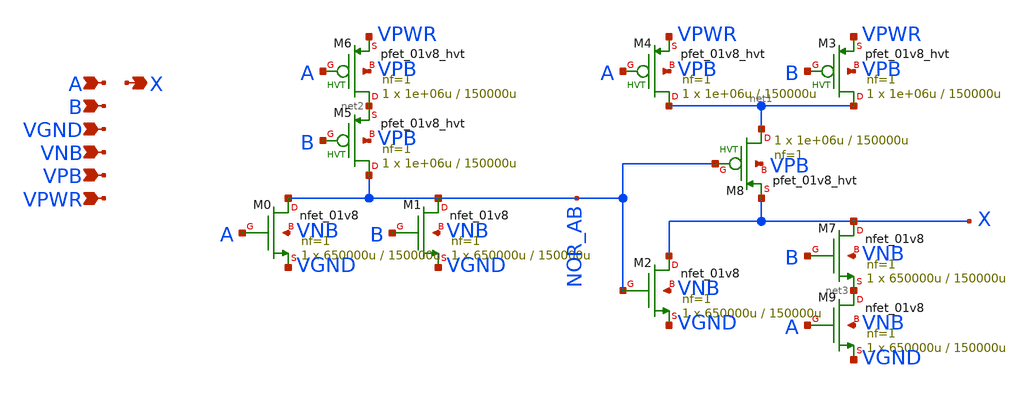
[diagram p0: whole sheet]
** sch_path: schematics/xor2/sky130_fd_sc_hd__xor2_1.sch
**.subckt sky130_fd_sc_hd__xor2_1 A B VGND VNB VPB VPWR X
*.ipin A
*.ipin B
*.ipin VGND
*.ipin VNB
*.ipin VPB
*.ipin VPWR
*.opin X
XM4 net1 A VPWR VPB sky130_fd_pr__pfet_01v8_hvt L=150000u W=1e+06u nf=1 ad='int((1 + 1)/2) * 1e+06u / 1 * 0.29'
+ as='int((1 + 2)/2) * 1e+06u / 1 * 0.29' pd='2*int((1 + 1)/2) * (1e+06u / 1 + 0.29)' ps='2*int((1 + 2)/2) * (1e+06u / 1 + 0.29)'
+ nrd='0.29 / 1e+06u ' nrs='0.29 / 1e+06u ' sa=0 sb=0 sd=0 mult=1 m=1
XM6 net2 A VPWR VPB sky130_fd_pr__pfet_01v8_hvt L=150000u W=1e+06u nf=1 ad='int((1 + 1)/2) * 1e+06u / 1 * 0.29'
+ as='int((1 + 2)/2) * 1e+06u / 1 * 0.29' pd='2*int((1 + 1)/2) * (1e+06u / 1 + 0.29)' ps='2*int((1 + 2)/2) * (1e+06u / 1 + 0.29)'
+ nrd='0.29 / 1e+06u ' nrs='0.29 / 1e+06u ' sa=0 sb=0 sd=0 mult=1 m=1
XM8 net1 NOR_AB X VPB sky130_fd_pr__pfet_01v8_hvt L=150000u W=1e+06u nf=1 ad='int((1 + 1)/2) * 1e+06u / 1 * 0.29'
+ as='int((1 + 2)/2) * 1e+06u / 1 * 0.29' pd='2*int((1 + 1)/2) * (1e+06u / 1 + 0.29)' ps='2*int((1 + 2)/2) * (1e+06u / 1 + 0.29)'
+ nrd='0.29 / 1e+06u ' nrs='0.29 / 1e+06u ' sa=0 sb=0 sd=0 mult=1 m=1
XM3 net1 B VPWR VPB sky130_fd_pr__pfet_01v8_hvt L=150000u W=1e+06u nf=1 ad='int((1 + 1)/2) * 1e+06u / 1 * 0.29'
+ as='int((1 + 2)/2) * 1e+06u / 1 * 0.29' pd='2*int((1 + 1)/2) * (1e+06u / 1 + 0.29)' ps='2*int((1 + 2)/2) * (1e+06u / 1 + 0.29)'
+ nrd='0.29 / 1e+06u ' nrs='0.29 / 1e+06u ' sa=0 sb=0 sd=0 mult=1 m=1
XM5 NOR_AB B net2 VPB sky130_fd_pr__pfet_01v8_hvt L=150000u W=1e+06u nf=1 ad='int((1 + 1)/2) * 1e+06u / 1 * 0.29'
+ as='int((1 + 2)/2) * 1e+06u / 1 * 0.29' pd='2*int((1 + 1)/2) * (1e+06u / 1 + 0.29)' ps='2*int((1 + 2)/2) * (1e+06u / 1 + 0.29)'
+ nrd='0.29 / 1e+06u ' nrs='0.29 / 1e+06u ' sa=0 sb=0 sd=0 mult=1 m=1
XM0 NOR_AB A VGND VNB sky130_fd_pr__nfet_01v8 L=150000u W=650000u nf=1 ad='int((1 + 1)/2) * 650000u / 1 * 0.29'
+ as='int((1 + 2)/2) * 650000u / 1 * 0.29' pd='2*int((1 + 1)/2) * (650000u / 1 + 0.29)' ps='2*int((1 + 2)/2) * (650000u / 1 + 0.29)'
+ nrd='0.29 / 650000u ' nrs='0.29 / 650000u ' sa=0 sb=0 sd=0 mult=1 m=1
XM9 net3 A VGND VNB sky130_fd_pr__nfet_01v8 L=150000u W=650000u nf=1 ad='int((1 + 1)/2) * 650000u / 1 * 0.29'
+ as='int((1 + 2)/2) * 650000u / 1 * 0.29' pd='2*int((1 + 1)/2) * (650000u / 1 + 0.29)' ps='2*int((1 + 2)/2) * (650000u / 1 + 0.29)'
+ nrd='0.29 / 650000u ' nrs='0.29 / 650000u ' sa=0 sb=0 sd=0 mult=1 m=1
XM2 X NOR_AB VGND VNB sky130_fd_pr__nfet_01v8 L=150000u W=650000u nf=1 ad='int((1 + 1)/2) * 650000u / 1 * 0.29'
+ as='int((1 + 2)/2) * 650000u / 1 * 0.29' pd='2*int((1 + 1)/2) * (650000u / 1 + 0.29)' ps='2*int((1 + 2)/2) * (650000u / 1 + 0.29)'
+ nrd='0.29 / 650000u ' nrs='0.29 / 650000u ' sa=0 sb=0 sd=0 mult=1 m=1
XM1 NOR_AB B VGND VNB sky130_fd_pr__nfet_01v8 L=150000u W=650000u nf=1 ad='int((1 + 1)/2) * 650000u / 1 * 0.29'
+ as='int((1 + 2)/2) * 650000u / 1 * 0.29' pd='2*int((1 + 1)/2) * (650000u / 1 + 0.29)' ps='2*int((1 + 2)/2) * (650000u / 1 + 0.29)'
+ nrd='0.29 / 650000u ' nrs='0.29 / 650000u ' sa=0 sb=0 sd=0 mult=1 m=1
XM7 X B net3 VNB sky130_fd_pr__nfet_01v8 L=150000u W=650000u nf=1 ad='int((1 + 1)/2) * 650000u / 1 * 0.29'
+ as='int((1 + 2)/2) * 650000u / 1 * 0.29' pd='2*int((1 + 1)/2) * (650000u / 1 + 0.29)' ps='2*int((1 + 2)/2) * (650000u / 1 + 0.29)'
+ nrd='0.29 / 650000u ' nrs='0.29 / 650000u ' sa=0 sb=0 sd=0 mult=1 m=1
**.ends
.end
